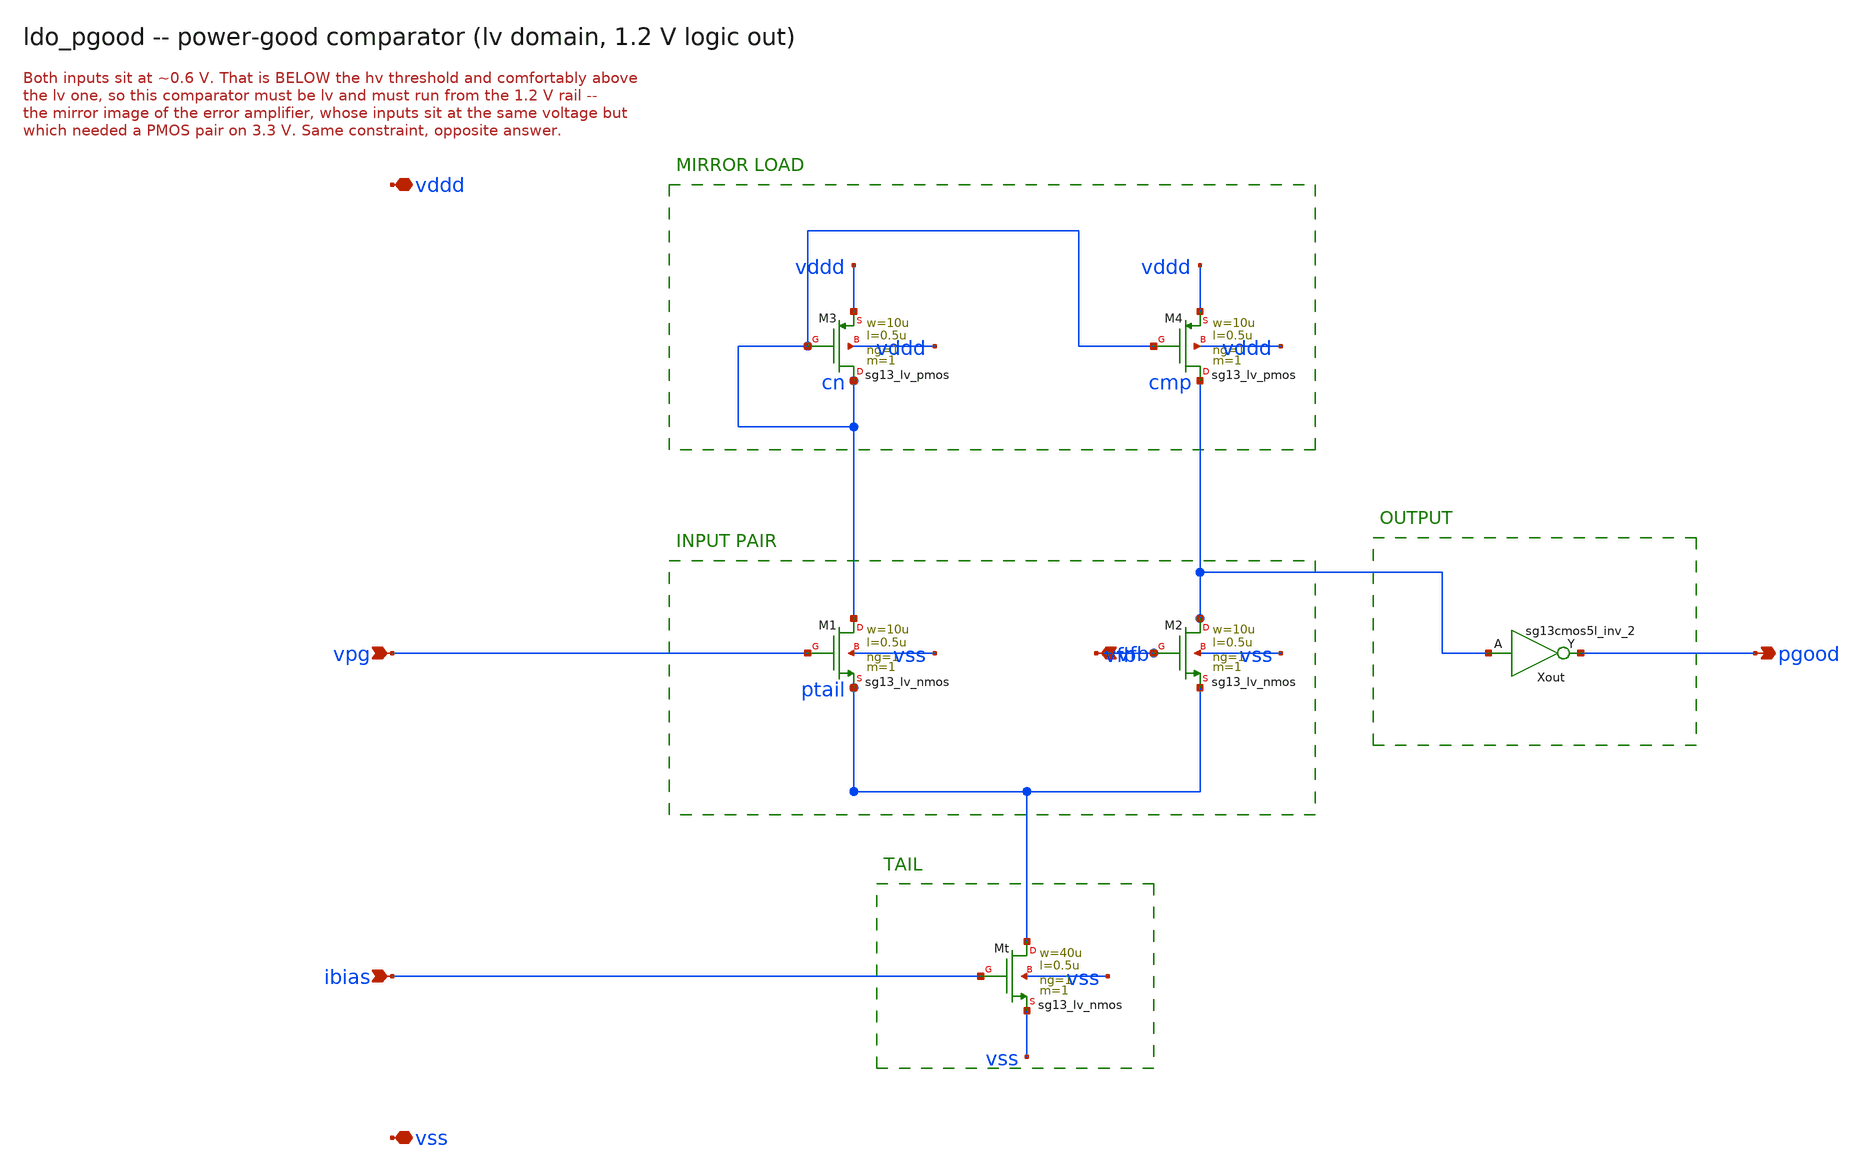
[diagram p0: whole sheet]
** sch_path: xschem/ldo_pgood.sch
**.subckt ldo_pgood vfb vpg ibias pgood vddd vss
*.ipin vfb
*.ipin vpg
*.ipin ibias
*.opin pgood
*.iopin vddd
*.iopin vss
XM1 cn vpg ptail vss sg13_lv_nmos w=10u l=0.5u ng=1 m=1 mm_ok=1
XM2 cmp vfb ptail vss sg13_lv_nmos w=10u l=0.5u ng=1 m=1 mm_ok=1
XM3 cn cn vddd vddd sg13_lv_pmos w=10u l=0.5u ng=1 m=1 mm_ok=1
XM4 cmp cn vddd vddd sg13_lv_pmos w=10u l=0.5u ng=1 m=1 mm_ok=1
XMt ptail ibias vss vss sg13_lv_nmos w=40u l=0.5u ng=1 m=1 mm_ok=1
Xout pgood cmp vddd vss sg13cmos5l_inv_2
**.ends
.end
